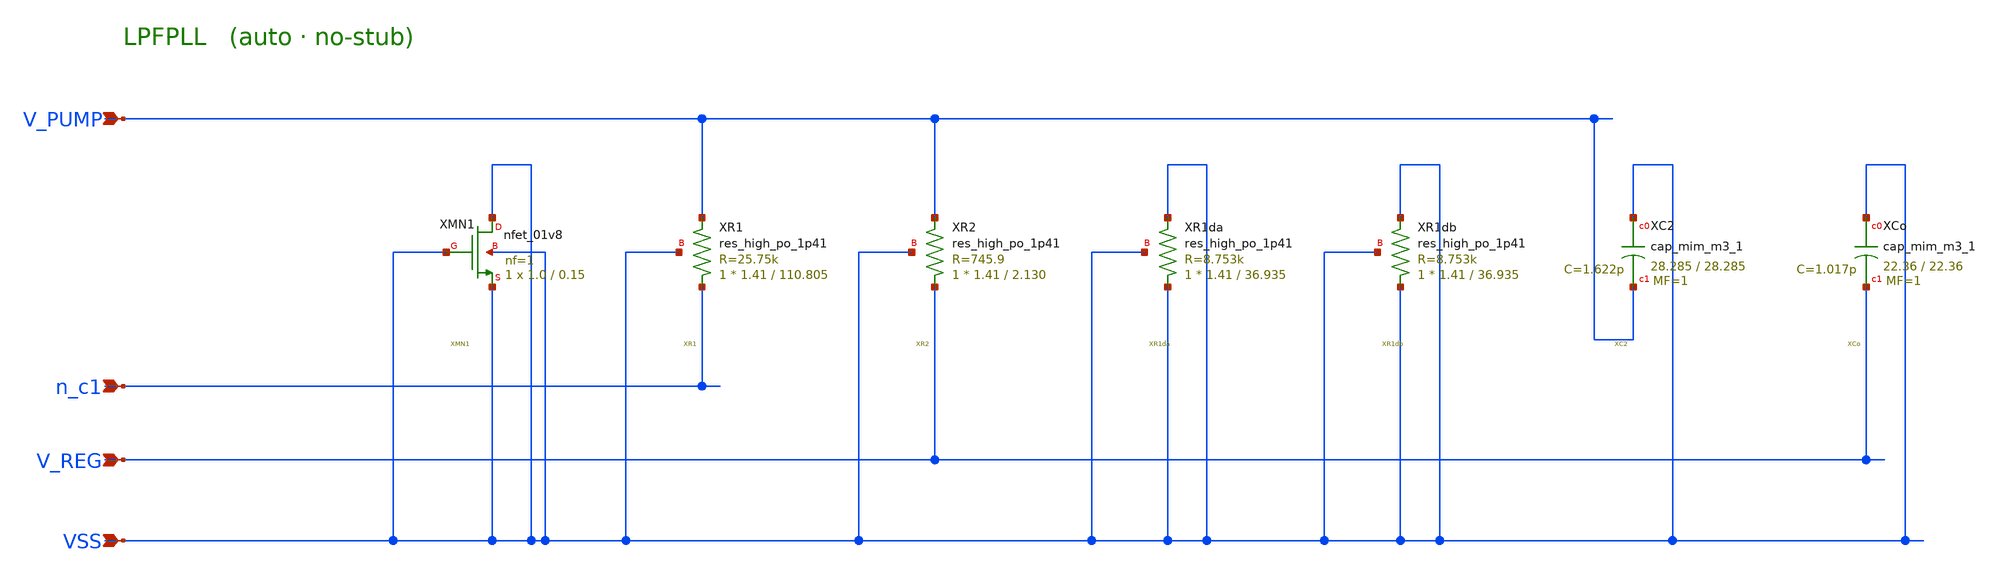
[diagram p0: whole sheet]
** sch_path: schematics/LPFPLL.sch
**.subckt LPFPLL VSS V_PUMP V_REG n_c1
*.ipin VSS
*.ipin V_PUMP
*.ipin V_REG
*.ipin n_c1
XXMN1 VSS VSS VSS VSS sky130_fd_pr__nfet_01v8 L=0.15 W=1.0 nf=1 ad='int((1 + 1)/2) * 1.0 / 1 * 0.29'
+ as='int((1 + 2)/2) * 1.0 / 1 * 0.29' pd='2*int((1 + 1)/2) * (1.0 / 1 + 0.29)' ps='2*int((1 + 2)/2) * (1.0 / 1 + 0.29)'
+ nrd='0.29 / 1.0 ' nrs='0.29 / 1.0 ' sa=0 sb=0 sd=0 mult=1 m=1
XXR1 n_c1 V_PUMP VSS sky130_fd_pr__res_high_po_1p41 L=110.805 mult=1 m=1
XXR2 V_REG V_PUMP VSS sky130_fd_pr__res_high_po_1p41 L=2.130 mult=1 m=1
XXR1da VSS VSS VSS sky130_fd_pr__res_high_po_1p41 L=36.935 mult=1 m=1
XXR1db VSS VSS VSS sky130_fd_pr__res_high_po_1p41 L=36.935 mult=1 m=1
XXC2 VSS V_PUMP sky130_fd_pr__cap_mim_m3_1 W=28.285 L=28.285 MF=1 m=1
XXCo VSS V_REG sky130_fd_pr__cap_mim_m3_1 W=22.36 L=22.36 MF=1 m=1
**.ends
.end
